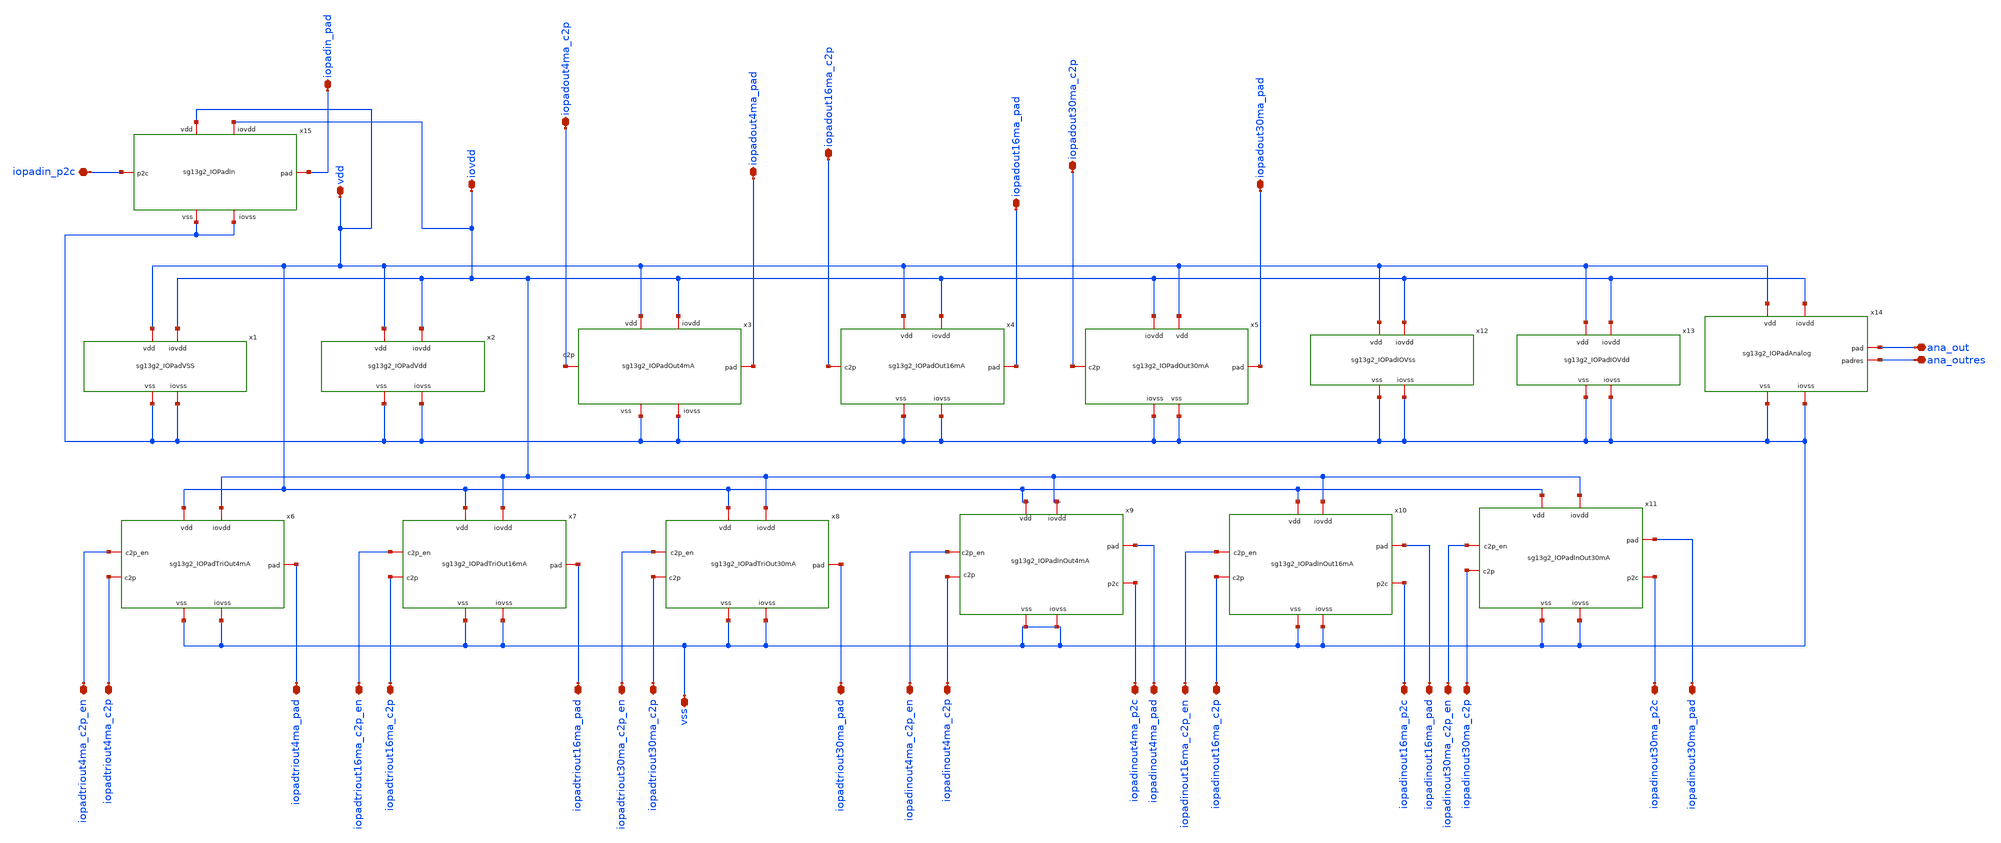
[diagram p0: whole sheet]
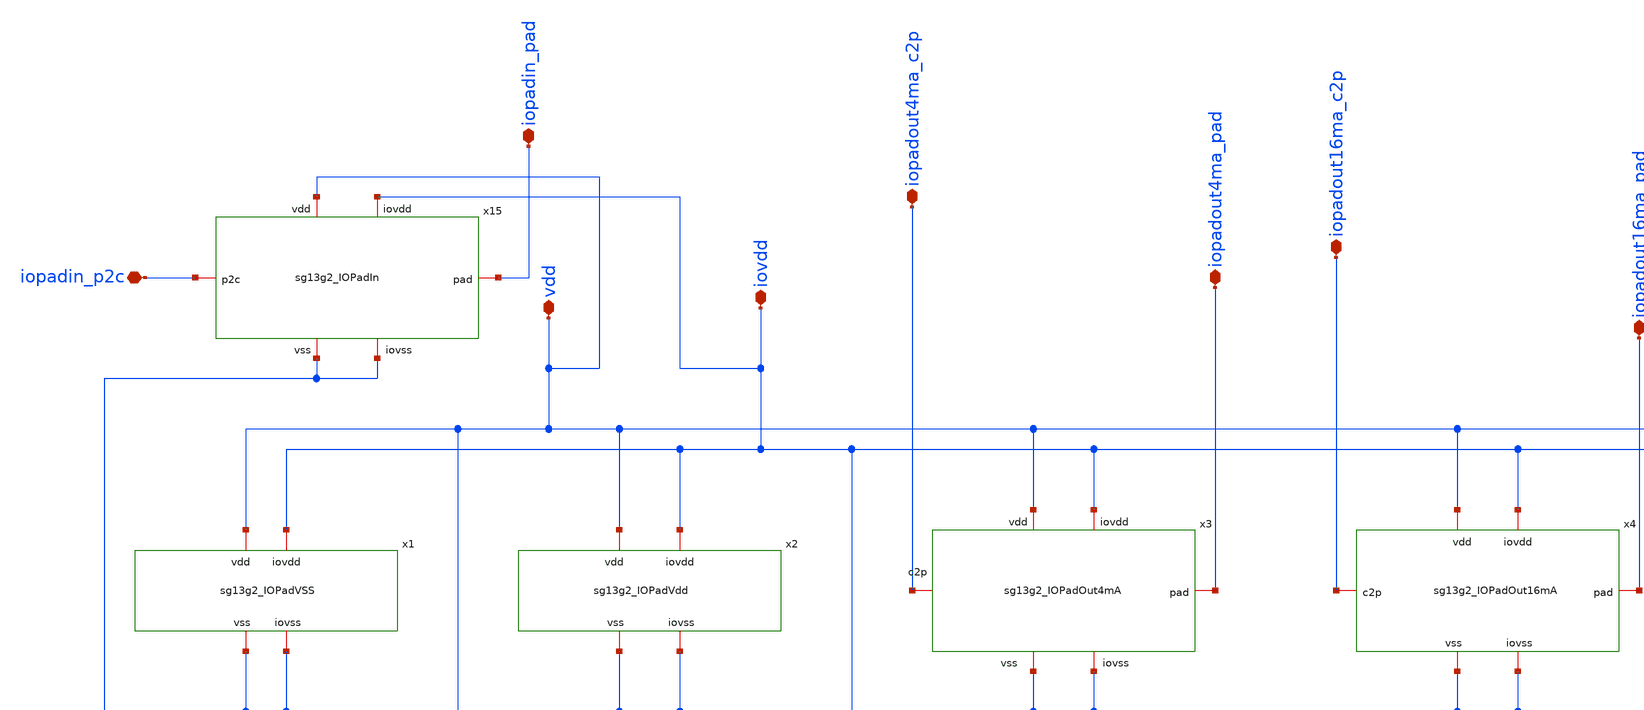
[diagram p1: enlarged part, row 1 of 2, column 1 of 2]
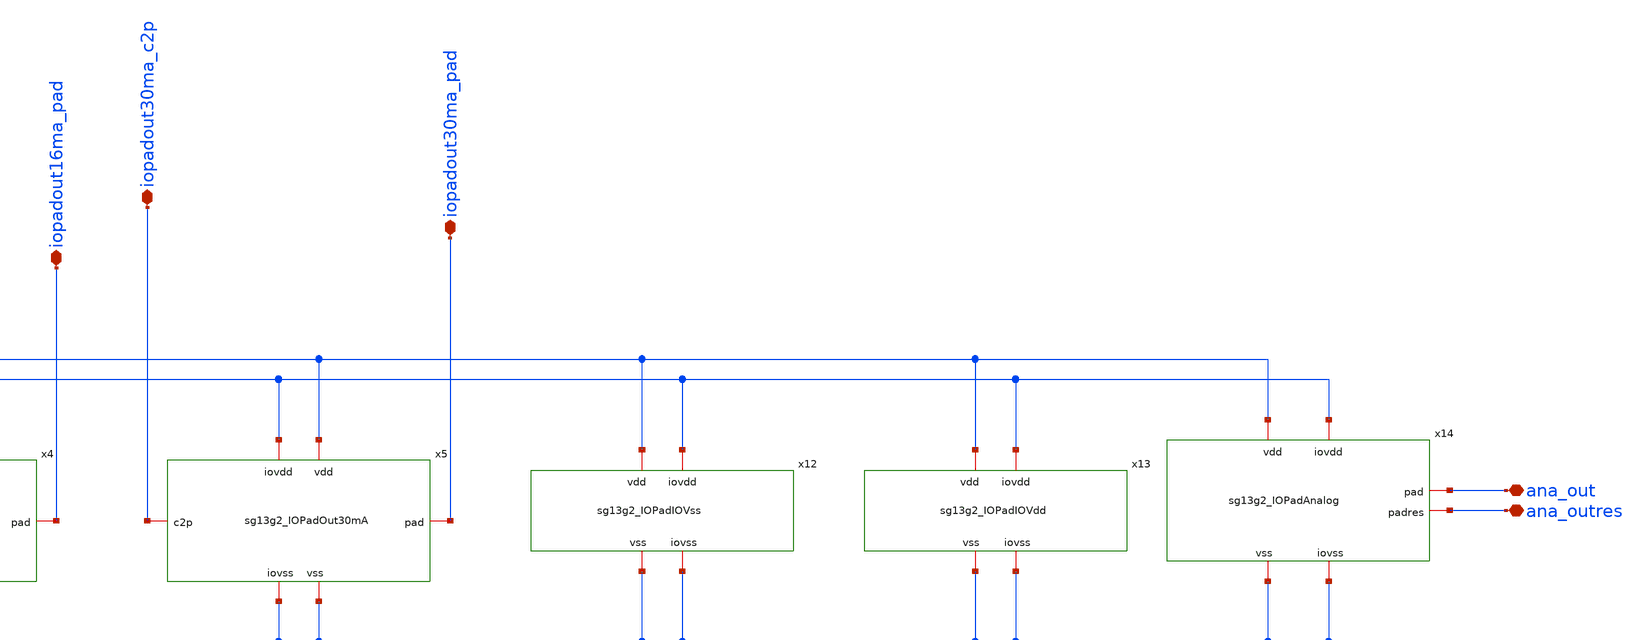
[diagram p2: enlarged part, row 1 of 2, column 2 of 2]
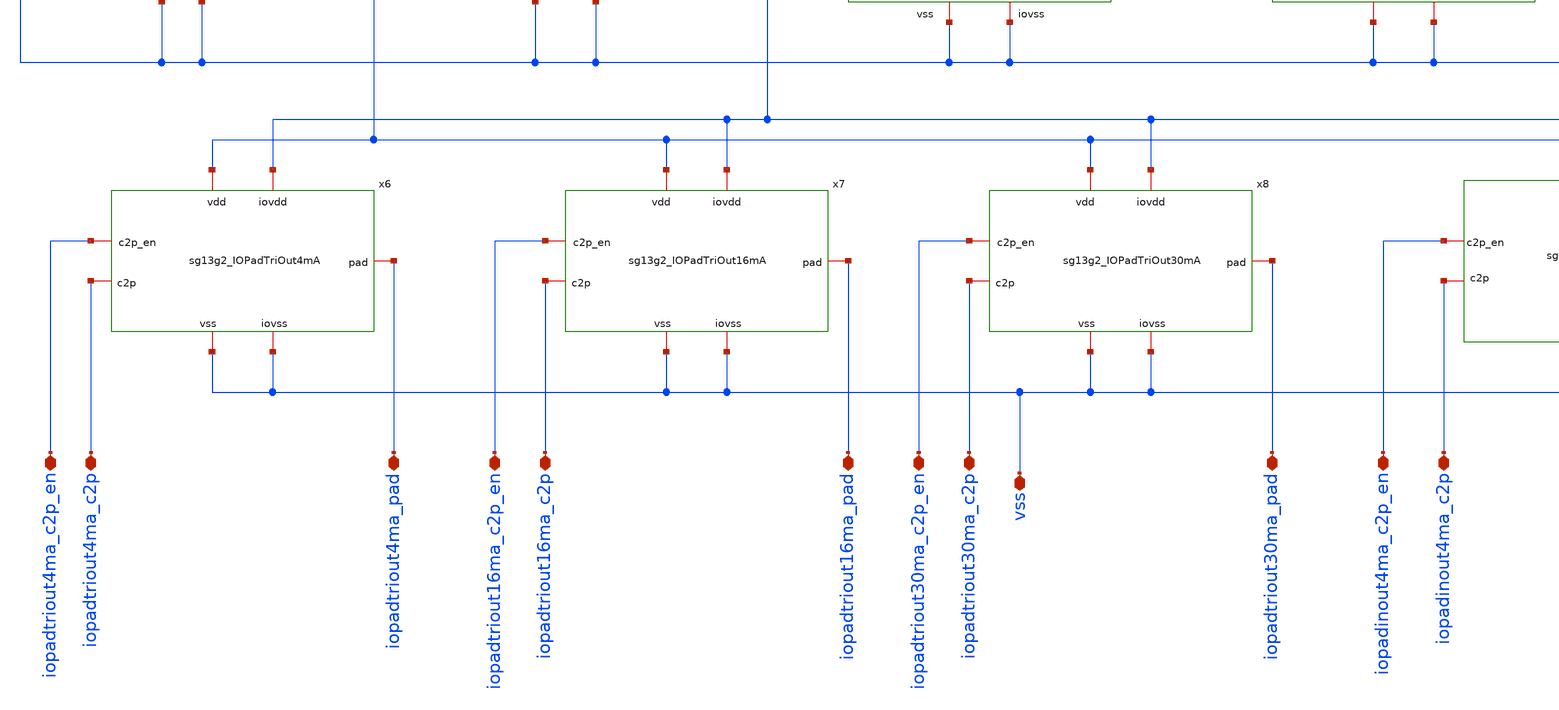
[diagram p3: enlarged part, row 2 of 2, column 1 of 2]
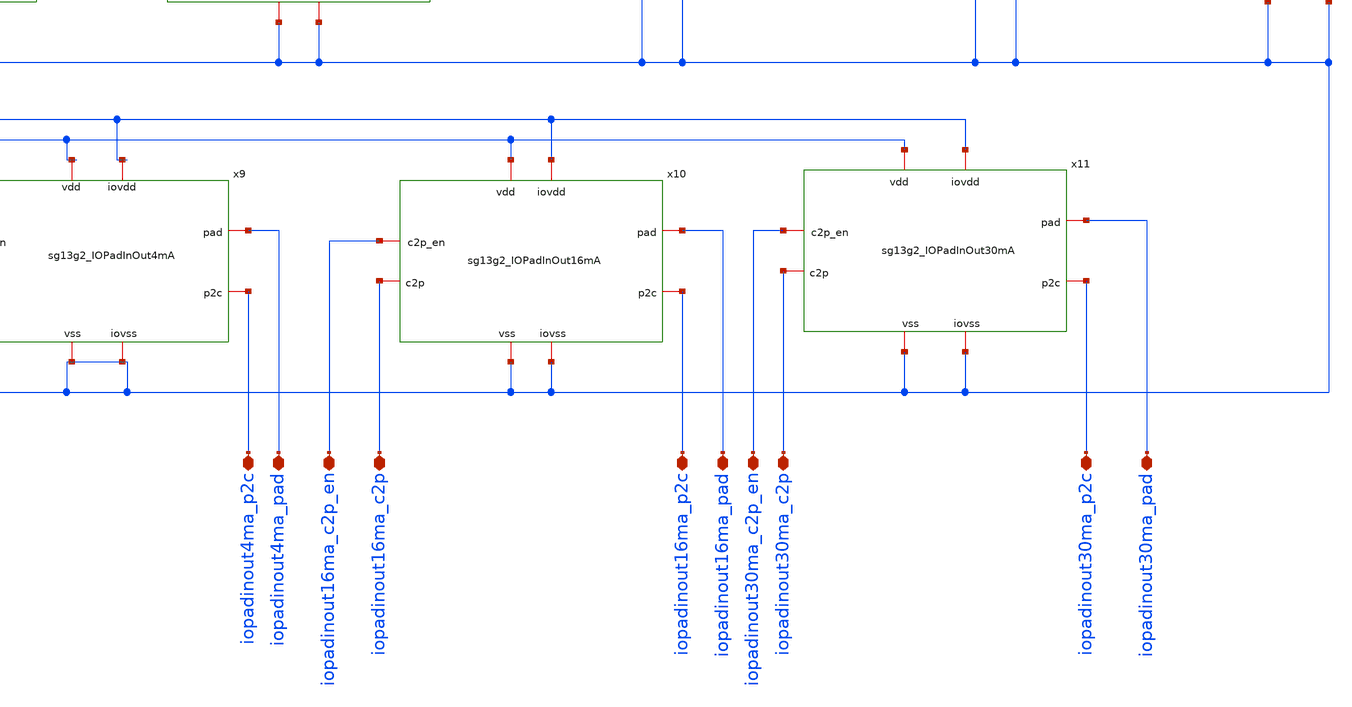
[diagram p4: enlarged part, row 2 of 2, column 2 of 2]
** sch_path: ihp-sg13g2/libs.ref/sg13g2_io/xschem/sg13g2_Gallery.sch
**.subckt sg13g2_Gallery vdd iovdd vss iopadin_pad iopadout4ma_pad iopadout16ma_pad iopadout30ma_pad
*+ iopadtriout4ma_pad iopadtriout16ma_pad iopadtriout30ma_pad iopadinout4ma_pad iopadinout16ma_pad iopadinout30ma_pad
*+ iopadin_p2c iopadout4ma_c2p iopadout16ma_c2p iopadout30ma_c2p iopadinout4ma_p2c iopadinout16ma_p2c
*+ iopadinout30ma_p2c iopadtriout4ma_c2p iopadtriout4ma_c2p_en iopadtriout16ma_c2p iopadtriout16ma_c2p_en
*+ iopadtriout30ma_c2p iopadtriout30ma_c2p_en iopadinout4ma_c2p iopadinout4ma_c2p_en iopadinout16ma_c2p
*+ iopadinout16ma_c2p_en iopadinout30ma_c2p iopadinout30ma_c2p_en ana_out ana_outres
*.iopin vdd
*.iopin iovdd
*.iopin vss
*.iopin iopadin_pad
*.iopin iopadout4ma_pad
*.iopin iopadout16ma_pad
*.iopin iopadout30ma_pad
*.iopin iopadtriout4ma_pad
*.iopin iopadtriout16ma_pad
*.iopin iopadtriout30ma_pad
*.iopin iopadinout4ma_pad
*.iopin iopadinout16ma_pad
*.iopin iopadinout30ma_pad
*.iopin iopadin_p2c
*.iopin iopadout4ma_c2p
*.iopin iopadout16ma_c2p
*.iopin iopadout30ma_c2p
*.iopin iopadinout4ma_p2c
*.iopin iopadinout16ma_p2c
*.iopin iopadinout30ma_p2c
*.iopin iopadtriout4ma_c2p
*.iopin iopadtriout4ma_c2p_en
*.iopin iopadtriout16ma_c2p
*.iopin iopadtriout16ma_c2p_en
*.iopin iopadtriout30ma_c2p
*.iopin iopadtriout30ma_c2p_en
*.iopin iopadinout4ma_c2p
*.iopin iopadinout4ma_c2p_en
*.iopin iopadinout16ma_c2p
*.iopin iopadinout16ma_c2p_en
*.iopin iopadinout30ma_c2p
*.iopin iopadinout30ma_c2p_en
*.iopin ana_out
*.iopin ana_outres
x1 vdd iovdd vss vss sg13g2_IOPadVSS
x2 vdd iovdd vss vss sg13g2_IOPadVdd
x3 iovdd vdd iopadout4ma_pad iopadout4ma_c2p vss vss sg13g2_IOPadOut4mA
x4 iovdd vdd iopadout16ma_pad iopadout16ma_c2p vss vss sg13g2_IOPadOut16mA
x5 iovdd vdd iopadout30ma_pad iopadout30ma_c2p vss vss sg13g2_IOPadOut30mA
x6 iovdd vdd iopadtriout4ma_pad iopadtriout4ma_c2p_en iopadtriout4ma_c2p vss vss
+ sg13g2_IOPadTriOut4mA
x7 iovdd vdd iopadtriout16ma_pad iopadtriout16ma_c2p_en iopadtriout16ma_c2p vss vss
+ sg13g2_IOPadTriOut16mA
x8 iovdd vdd iopadtriout30ma_pad iopadtriout30ma_c2p_en iopadtriout30ma_c2p vss vss
+ sg13g2_IOPadTriOut30mA
x9 iovdd vdd iopadinout4ma_pad iopadinout4ma_c2p_en iopadinout4ma_c2p iopadinout4ma_p2c vss vss
+ sg13g2_IOPadInOut4mA
x10 iovdd vdd iopadinout16ma_pad iopadinout16ma_c2p_en iopadinout16ma_c2p iopadinout16ma_p2c vss vss
+ sg13g2_IOPadInOut16mA
x11 iovdd vdd iopadinout30ma_pad iopadinout30ma_c2p_en iopadinout30ma_c2p iopadinout30ma_p2c vss vss
+ sg13g2_IOPadInOut30mA
x12 vdd iovdd vss vss sg13g2_IOPadIOVss
x13 iovdd vdd vss vss sg13g2_IOPadIOVdd
x14 vdd iovdd ana_out ana_outres vss vss sg13g2_IOPadAnalog
x15 iovdd vdd iopadin_pad iopadin_p2c vss vss sg13g2_IOPadIn
**.ends
.end
